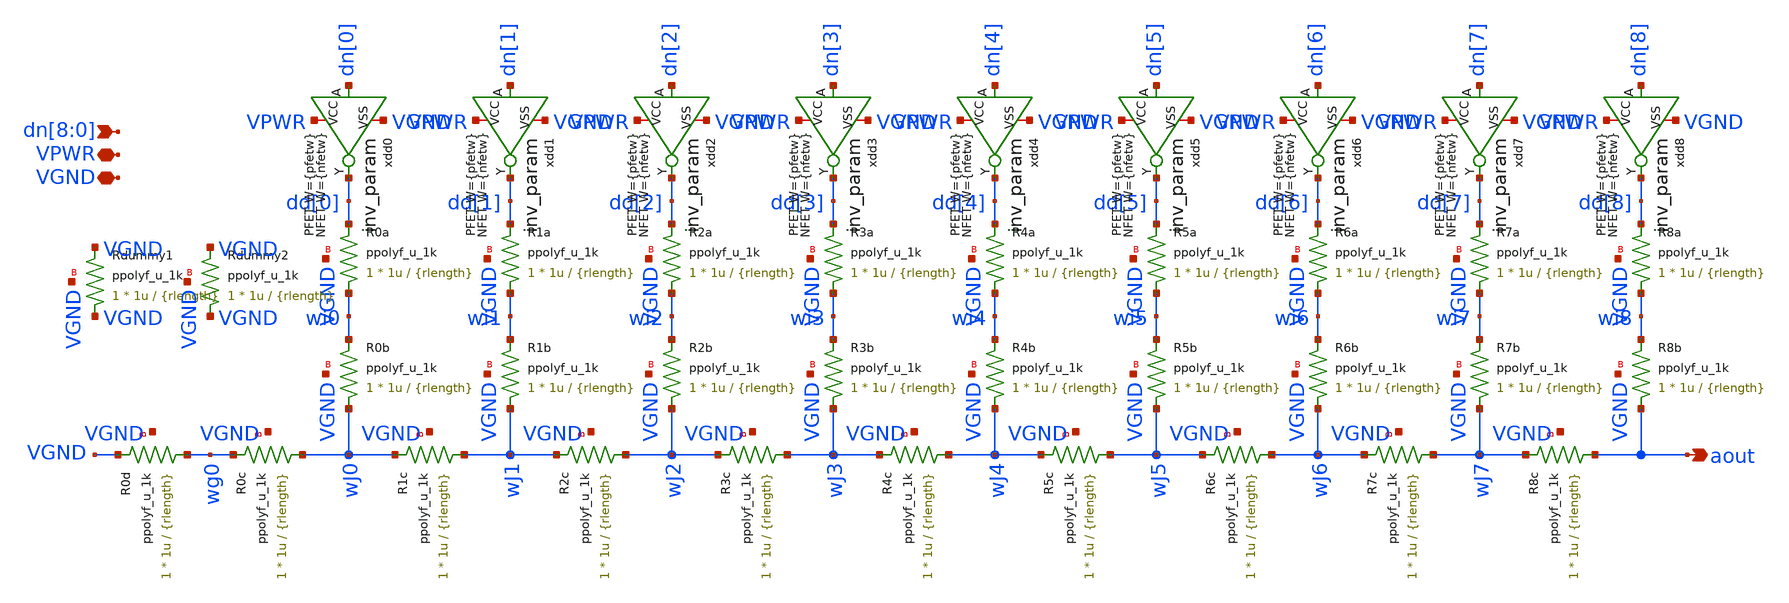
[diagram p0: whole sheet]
** sch_path: xschem/r2r_dac_param.sch
**.subckt r2r_dac_param VGND aout dn[8],dn[7],dn[6],dn[5],dn[4],dn[3],dn[2],dn[1],dn[0] VPWR
*.iopin VGND
*.opin aout
*.ipin dn[8],dn[7],dn[6],dn[5],dn[4],dn[3],dn[2],dn[1],dn[0]
*.iopin VPWR
XR0a wi0 dd[0] VGND ppolyf_u_1k r_width=1u r_length={rlength} m=1
XR0b wJ0 wi0 VGND ppolyf_u_1k r_width=1u r_length={rlength} m=1
XR0c wJ0 wg0 VGND ppolyf_u_1k r_width=1u r_length={rlength} m=1
XR0d wg0 VGND VGND ppolyf_u_1k r_width=1u r_length={rlength} m=1
XR1a wi1 dd[1] VGND ppolyf_u_1k r_width=1u r_length={rlength} m=1
XR1b wJ1 wi1 VGND ppolyf_u_1k r_width=1u r_length={rlength} m=1
XR1c wJ1 wJ0 VGND ppolyf_u_1k r_width=1u r_length={rlength} m=1
XR2a wi2 dd[2] VGND ppolyf_u_1k r_width=1u r_length={rlength} m=1
XR2b wJ2 wi2 VGND ppolyf_u_1k r_width=1u r_length={rlength} m=1
XR2c wJ2 wJ1 VGND ppolyf_u_1k r_width=1u r_length={rlength} m=1
XR3a wi3 dd[3] VGND ppolyf_u_1k r_width=1u r_length={rlength} m=1
XR3b wJ3 wi3 VGND ppolyf_u_1k r_width=1u r_length={rlength} m=1
XR3c wJ3 wJ2 VGND ppolyf_u_1k r_width=1u r_length={rlength} m=1
XR4a wi4 dd[4] VGND ppolyf_u_1k r_width=1u r_length={rlength} m=1
XR4b wJ4 wi4 VGND ppolyf_u_1k r_width=1u r_length={rlength} m=1
XR4c wJ4 wJ3 VGND ppolyf_u_1k r_width=1u r_length={rlength} m=1
XR5a wi5 dd[5] VGND ppolyf_u_1k r_width=1u r_length={rlength} m=1
XR5b wJ5 wi5 VGND ppolyf_u_1k r_width=1u r_length={rlength} m=1
XR5c wJ5 wJ4 VGND ppolyf_u_1k r_width=1u r_length={rlength} m=1
XR6a wi6 dd[6] VGND ppolyf_u_1k r_width=1u r_length={rlength} m=1
XR6b wJ6 wi6 VGND ppolyf_u_1k r_width=1u r_length={rlength} m=1
XR6c wJ6 wJ5 VGND ppolyf_u_1k r_width=1u r_length={rlength} m=1
XR7a wi7 dd[7] VGND ppolyf_u_1k r_width=1u r_length={rlength} m=1
XR7b wJ7 wi7 VGND ppolyf_u_1k r_width=1u r_length={rlength} m=1
XR7c wJ7 wJ6 VGND ppolyf_u_1k r_width=1u r_length={rlength} m=1
XR8a wi8 dd[8] VGND ppolyf_u_1k r_width=1u r_length={rlength} m=1
XR8b aout wi8 VGND ppolyf_u_1k r_width=1u r_length={rlength} m=1
XR8c aout wJ7 VGND ppolyf_u_1k r_width=1u r_length={rlength} m=1
XRdummy1 VGND VGND VGND ppolyf_u_1k r_width=1u r_length={rlength} m=1
XRdummy2 VGND VGND VGND ppolyf_u_1k r_width=1u r_length={rlength} m=1
xdd0 VPWR VGND dd[0] dn[0] inv_param pfetw={pfetw} nfetw={nfetw}
xdd1 VPWR VGND dd[1] dn[1] inv_param pfetw={pfetw} nfetw={nfetw}
xdd2 VPWR VGND dd[2] dn[2] inv_param pfetw={pfetw} nfetw={nfetw}
xdd3 VPWR VGND dd[3] dn[3] inv_param pfetw={pfetw} nfetw={nfetw}
xdd4 VPWR VGND dd[4] dn[4] inv_param pfetw={pfetw} nfetw={nfetw}
xdd5 VPWR VGND dd[5] dn[5] inv_param pfetw={pfetw} nfetw={nfetw}
xdd6 VPWR VGND dd[6] dn[6] inv_param pfetw={pfetw} nfetw={nfetw}
xdd7 VPWR VGND dd[7] dn[7] inv_param pfetw={pfetw} nfetw={nfetw}
xdd8 VPWR VGND dd[8] dn[8] inv_param pfetw={pfetw} nfetw={nfetw}
**.ends

* expanding   symbol:  inv_param.sym # of pins=4
** sym_path: xschem/inv_param.sym
** sch_path: xschem/inv_param.sch
.subckt inv_param VCC VSS Y A  pfetw=15u nfetw=4.5u
*.iopin VCC
*.iopin VSS
*.ipin A
*.opin Y
XMNi Y A VSS VSS nfet_03v3 L=0.28u W={nfetw} nf=1 ad='int((nf+1)/2) * W/nf * 0.18u' as='int((nf+2)/2) * W/nf * 0.18u'
+ pd='2*int((nf+1)/2) * (W/nf + 0.18u)' ps='2*int((nf+2)/2) * (W/nf + 0.18u)' nrd='0.18u / W' nrs='0.18u / W'
+ sa=0 sb=0 sd=0 m=1
XMPi Y A VCC VCC pfet_03v3 L=0.28u W={pfetw} nf=1 ad='int((nf+1)/2) * W/nf * 0.18u' as='int((nf+2)/2) * W/nf * 0.18u'
+ pd='2*int((nf+1)/2) * (W/nf + 0.18u)' ps='2*int((nf+2)/2) * (W/nf + 0.18u)' nrd='0.18u / W' nrs='0.18u / W'
+ sa=0 sb=0 sd=0 m=1
.ends

.end
